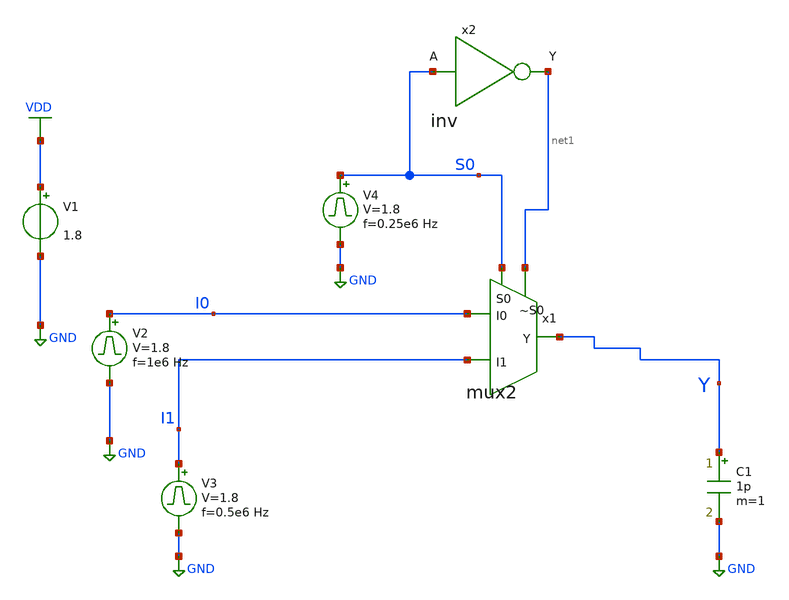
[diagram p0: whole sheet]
** sch_path: xschem/mux2_tb.sch
**.subckt mux2_tb
V1 VDD GND 1.8
V2 I0 GND pulse 0 1.8 '0.495/ 1e6 ' '0.01/1e6 ' '0.01/1e6 ' '0.49/1e6 ' '1/1e6 '
C1 Y GND 1p m=1
V3 I1 GND pulse 0 1.8 '0.495/ 0.5e6 ' '0.01/0.5e6 ' '0.01/0.5e6 ' '0.49/0.5e6 ' '1/0.5e6 '
V4 S0 GND pulse 0 1.8 '0.495/ 0.25e6 ' '0.01/0.25e6 ' '0.01/0.25e6 ' '0.49/0.25e6 ' '1/0.25e6 '
x1 I1 I0 S0 Y net1 mux2
x2 net1 S0 inv
**** begin user architecture code


.control
save all
tran 1n 8u
plot V(I0) V(I1)+2 V(S0)+4 V(Y)+6
.endc



** opencircuitdesign pdks install
.lib $::SKYWATER_MODELS/sky130.lib.spice tt


**** end user architecture code
**.ends
.GLOBAL VDD
.GLOBAL GND
.end
